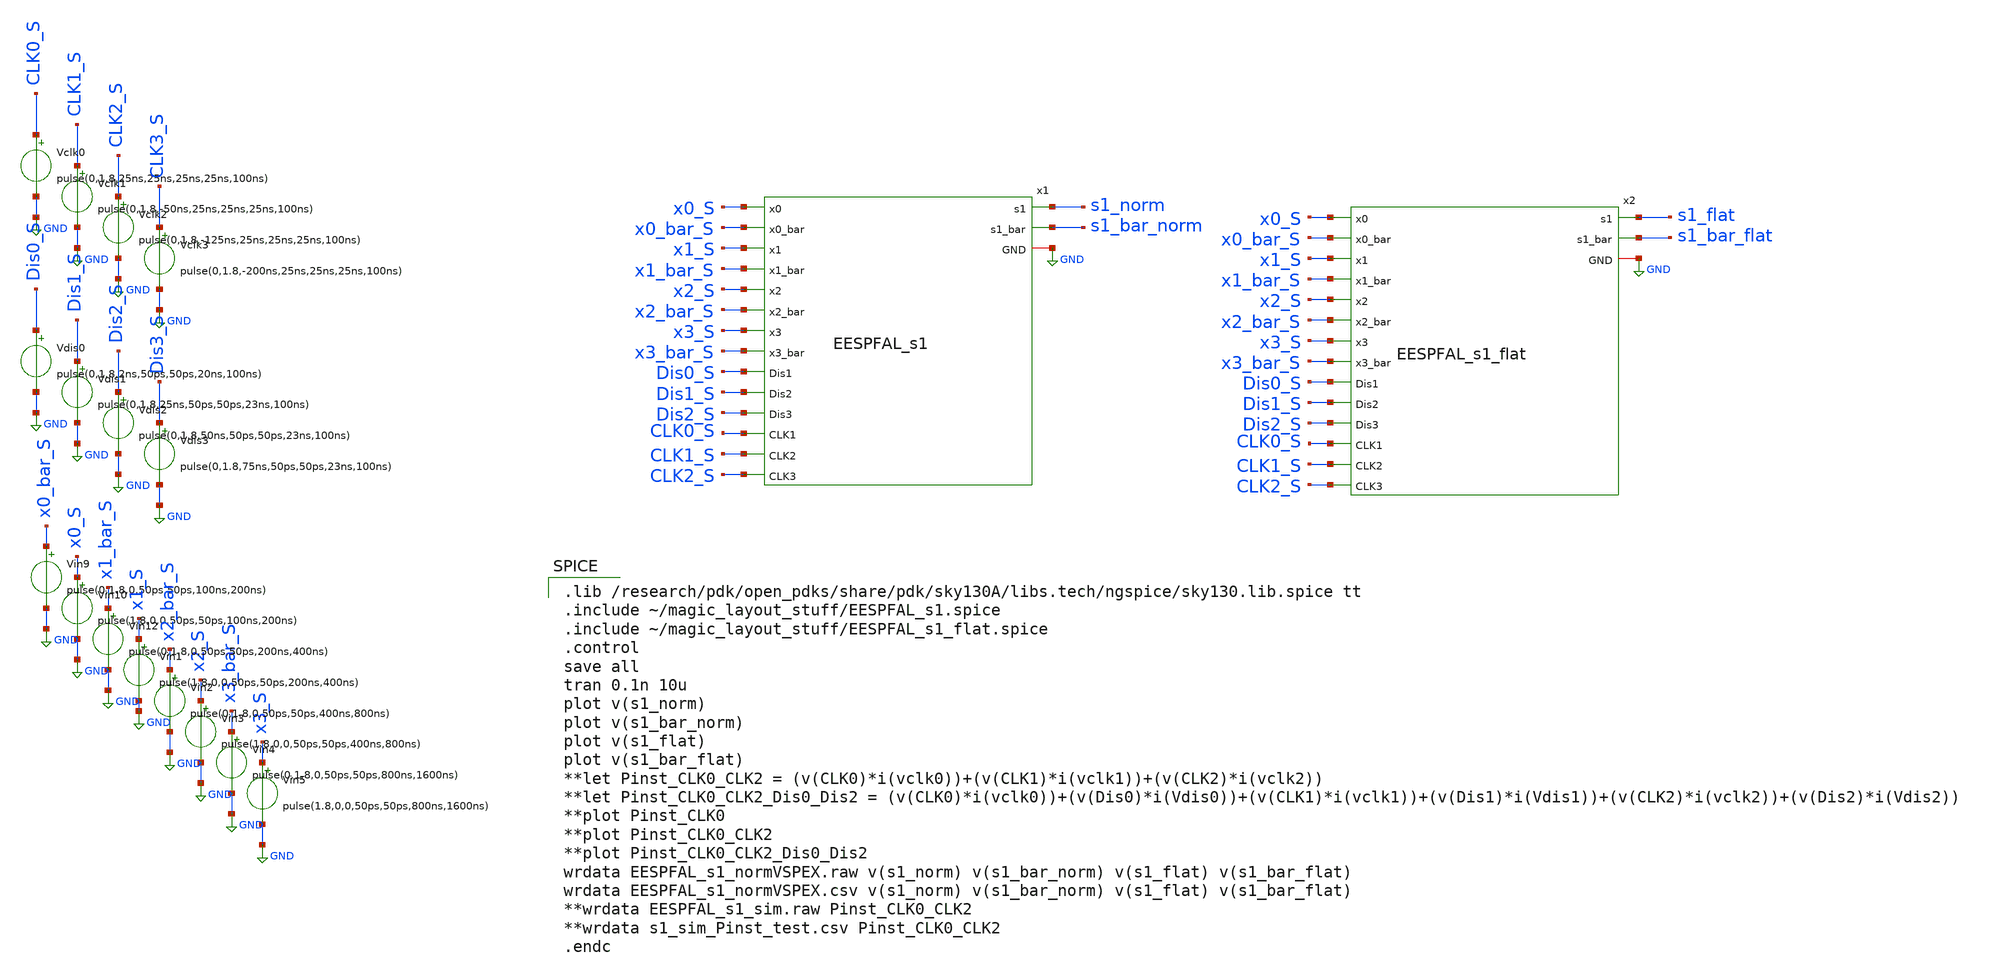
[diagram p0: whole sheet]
** sch_path: skywater_stuff/EESPFAL_s1_sim.sch
**.subckt EESPFAL_s1_sim
x1 GND x0_S x0_bar_S x1_S x1_bar_S x2_S x2_bar_S x3_S x3_bar_S s1_bar_norm s1_norm CLK0_S Dis0_S
+ Dis2_S CLK2_S Dis1_S CLK1_S EESPFAL_s1
Vin9 x0_bar_S GND pulse(0,1.8,0,50ps,50ps,100ns,200ns)
Vin10 x0_S GND pulse(1.8,0,0,50ps,50ps,100ns,200ns)
Vin12 x1_bar_S GND pulse(0,1.8,0,50ps,50ps,200ns,400ns)
Vin1 x1_S GND pulse(1.8,0,0,50ps,50ps,200ns,400ns)
Vin2 x2_bar_S GND pulse(0,1.8,0,50ps,50ps,400ns,800ns)
Vin3 x2_S GND pulse(1.8,0,0,50ps,50ps,400ns,800ns)
Vin4 x3_bar_S GND pulse(0,1.8,0,50ps,50ps,800ns,1600ns)
Vin5 x3_S GND pulse(1.8,0,0,50ps,50ps,800ns,1600ns)
Vdis0 Dis0_S GND pulse(0,1.8,2ns,50ps,50ps,20ns,100ns)
Vclk0 CLK0_S GND pulse(0,1.8,25ns,25ns,25ns,25ns,100ns)
Vdis1 Dis1_S GND pulse(0,1.8,25ns,50ps,50ps,23ns,100ns)
Vdis2 Dis2_S GND pulse(0,1.8,50ns,50ps,50ps,23ns,100ns)
Vdis3 Dis3_S GND pulse(0,1.8,75ns,50ps,50ps,23ns,100ns)
Vclk1 CLK1_S GND pulse(0,1.8,-50ns,25ns,25ns,25ns,100ns)
Vclk2 CLK2_S GND pulse(0,1.8,-125ns,25ns,25ns,25ns,100ns)
Vclk3 CLK3_S GND pulse(0,1.8,-200ns,25ns,25ns,25ns,100ns)
x2 GND x0_S x0_bar_S x1_S x1_bar_S x2_S x2_bar_S x3_S x3_bar_S s1_bar_flat s1_flat Dis0_S Dis2_S
+ Dis1_S CLK0_S CLK1_S CLK2_S EESPFAL_s1_flat
**** begin user architecture code

.lib /research/pdk/open_pdks/share/pdk/sky130A/libs.tech/ngspice/sky130.lib.spice tt
.include ~/magic_layout_stuff/EESPFAL_s1.spice
.include ~/magic_layout_stuff/EESPFAL_s1_flat.spice
.control
save all
tran 0.1n 10u
plot v(s1_norm)
plot v(s1_bar_norm)
plot v(s1_flat)
plot v(s1_bar_flat)
**let Pinst_CLK0_CLK2 = (v(CLK0)*i(vclk0))+(v(CLK1)*i(vclk1))+(v(CLK2)*i(vclk2))
**let Pinst_CLK0_CLK2_Dis0_Dis2 =
*+ (v(CLK0)*i(vclk0))+(v(Dis0)*i(Vdis0))+(v(CLK1)*i(vclk1))+(v(Dis1)*i(Vdis1))+(v(CLK2)*i(vclk2))+(v(Dis2)*i(Vdis2))
**plot Pinst_CLK0
**plot Pinst_CLK0_CLK2
**plot Pinst_CLK0_CLK2_Dis0_Dis2
wrdata EESPFAL_s1_normVSPEX.raw v(s1_norm) v(s1_bar_norm) v(s1_flat) v(s1_bar_flat)
wrdata EESPFAL_s1_normVSPEX.csv v(s1_norm) v(s1_bar_norm) v(s1_flat) v(s1_bar_flat)
**wrdata EESPFAL_s1_sim.raw Pinst_CLK0_CLK2
**wrdata s1_sim_Pinst_test.csv Pinst_CLK0_CLK2
.endc


**** end user architecture code
**.ends
.GLOBAL GND
.end
